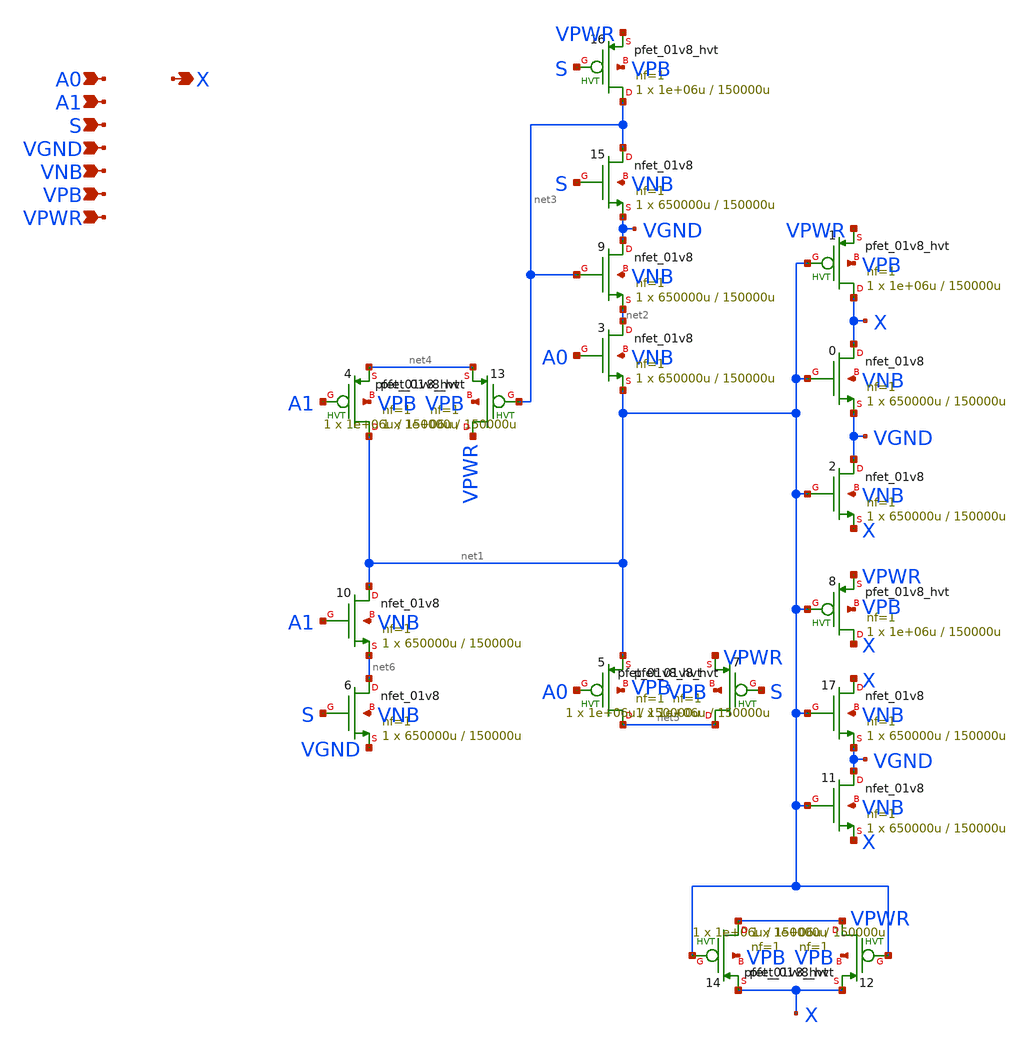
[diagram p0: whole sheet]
** sch_path: schematics/mux2/sky130_fd_sc_hd__mux2_4.sch
**.subckt sky130_fd_sc_hd__mux2_4 A0 A1 S VGND VNB VPB VPWR X
*.ipin A0
*.ipin A1
*.ipin S
*.ipin VGND
*.ipin VNB
*.ipin VPB
*.ipin VPWR
*.opin X
X0 X net1 VGND VNB sky130_fd_pr__nfet_01v8 L=150000u W=650000u nf=1 ad='int((1 + 1)/2) * 650000u / 1 * 0.29'
+ as='int((1 + 2)/2) * 650000u / 1 * 0.29' pd='2*int((1 + 1)/2) * (650000u / 1 + 0.29)' ps='2*int((1 + 2)/2) * (650000u / 1 + 0.29)'
+ nrd='0.29 / 650000u ' nrs='0.29 / 650000u ' sa=0 sb=0 sd=0 mult=1 m=1
X1 X net1 VPWR VPB sky130_fd_pr__pfet_01v8_hvt L=150000u W=1e+06u nf=1 ad='int((1 + 1)/2) * 1e+06u / 1 * 0.29'
+ as='int((1 + 2)/2) * 1e+06u / 1 * 0.29' pd='2*int((1 + 1)/2) * (1e+06u / 1 + 0.29)' ps='2*int((1 + 2)/2) * (1e+06u / 1 + 0.29)'
+ nrd='0.29 / 1e+06u ' nrs='0.29 / 1e+06u ' sa=0 sb=0 sd=0 mult=1 m=1
X2 VGND net1 X VNB sky130_fd_pr__nfet_01v8 L=150000u W=650000u nf=1 ad='int((1 + 1)/2) * 650000u / 1 * 0.29'
+ as='int((1 + 2)/2) * 650000u / 1 * 0.29' pd='2*int((1 + 1)/2) * (650000u / 1 + 0.29)' ps='2*int((1 + 2)/2) * (650000u / 1 + 0.29)'
+ nrd='0.29 / 650000u ' nrs='0.29 / 650000u ' sa=0 sb=0 sd=0 mult=1 m=1
X3 net2 A0 net1 VNB sky130_fd_pr__nfet_01v8 L=150000u W=650000u nf=1 ad='int((1 + 1)/2) * 650000u / 1 * 0.29'
+ as='int((1 + 2)/2) * 650000u / 1 * 0.29' pd='2*int((1 + 1)/2) * (650000u / 1 + 0.29)' ps='2*int((1 + 2)/2) * (650000u / 1 + 0.29)'
+ nrd='0.29 / 650000u ' nrs='0.29 / 650000u ' sa=0 sb=0 sd=0 mult=1 m=1
X4 net1 A1 net4 VPB sky130_fd_pr__pfet_01v8_hvt L=150000u W=1e+06u nf=1 ad='int((1 + 1)/2) * 1e+06u / 1 * 0.29'
+ as='int((1 + 2)/2) * 1e+06u / 1 * 0.29' pd='2*int((1 + 1)/2) * (1e+06u / 1 + 0.29)' ps='2*int((1 + 2)/2) * (1e+06u / 1 + 0.29)'
+ nrd='0.29 / 1e+06u ' nrs='0.29 / 1e+06u ' sa=0 sb=0 sd=0 mult=1 m=1
X9 VGND net3 net2 VNB sky130_fd_pr__nfet_01v8 L=150000u W=650000u nf=1 ad='int((1 + 1)/2) * 650000u / 1 * 0.29'
+ as='int((1 + 2)/2) * 650000u / 1 * 0.29' pd='2*int((1 + 1)/2) * (650000u / 1 + 0.29)' ps='2*int((1 + 2)/2) * (650000u / 1 + 0.29)'
+ nrd='0.29 / 650000u ' nrs='0.29 / 650000u ' sa=0 sb=0 sd=0 mult=1 m=1
X13 VPWR net3 net4 VPB sky130_fd_pr__pfet_01v8_hvt L=150000u W=1e+06u nf=1 ad='int((1 + 1)/2) * 1e+06u / 1 * 0.29'
+ as='int((1 + 2)/2) * 1e+06u / 1 * 0.29' pd='2*int((1 + 1)/2) * (1e+06u / 1 + 0.29)' ps='2*int((1 + 2)/2) * (1e+06u / 1 + 0.29)'
+ nrd='0.29 / 1e+06u ' nrs='0.29 / 1e+06u ' sa=0 sb=0 sd=0 mult=1 m=1
X15 net3 S VGND VNB sky130_fd_pr__nfet_01v8 L=150000u W=650000u nf=1 ad='int((1 + 1)/2) * 650000u / 1 * 0.29'
+ as='int((1 + 2)/2) * 650000u / 1 * 0.29' pd='2*int((1 + 1)/2) * (650000u / 1 + 0.29)' ps='2*int((1 + 2)/2) * (650000u / 1 + 0.29)'
+ nrd='0.29 / 650000u ' nrs='0.29 / 650000u ' sa=0 sb=0 sd=0 mult=1 m=1
X16 net3 S VPWR VPB sky130_fd_pr__pfet_01v8_hvt L=150000u W=1e+06u nf=1 ad='int((1 + 1)/2) * 1e+06u / 1 * 0.29'
+ as='int((1 + 2)/2) * 1e+06u / 1 * 0.29' pd='2*int((1 + 1)/2) * (1e+06u / 1 + 0.29)' ps='2*int((1 + 2)/2) * (1e+06u / 1 + 0.29)'
+ nrd='0.29 / 1e+06u ' nrs='0.29 / 1e+06u ' sa=0 sb=0 sd=0 mult=1 m=1
X5 net5 A0 net1 VPB sky130_fd_pr__pfet_01v8_hvt L=150000u W=1e+06u nf=1 ad='int((1 + 1)/2) * 1e+06u / 1 * 0.29'
+ as='int((1 + 2)/2) * 1e+06u / 1 * 0.29' pd='2*int((1 + 1)/2) * (1e+06u / 1 + 0.29)' ps='2*int((1 + 2)/2) * (1e+06u / 1 + 0.29)'
+ nrd='0.29 / 1e+06u ' nrs='0.29 / 1e+06u ' sa=0 sb=0 sd=0 mult=1 m=1
X7 net5 S VPWR VPB sky130_fd_pr__pfet_01v8_hvt L=150000u W=1e+06u nf=1 ad='int((1 + 1)/2) * 1e+06u / 1 * 0.29'
+ as='int((1 + 2)/2) * 1e+06u / 1 * 0.29' pd='2*int((1 + 1)/2) * (1e+06u / 1 + 0.29)' ps='2*int((1 + 2)/2) * (1e+06u / 1 + 0.29)'
+ nrd='0.29 / 1e+06u ' nrs='0.29 / 1e+06u ' sa=0 sb=0 sd=0 mult=1 m=1
X8 X net1 VPWR VPB sky130_fd_pr__pfet_01v8_hvt L=150000u W=1e+06u nf=1 ad='int((1 + 1)/2) * 1e+06u / 1 * 0.29'
+ as='int((1 + 2)/2) * 1e+06u / 1 * 0.29' pd='2*int((1 + 1)/2) * (1e+06u / 1 + 0.29)' ps='2*int((1 + 2)/2) * (1e+06u / 1 + 0.29)'
+ nrd='0.29 / 1e+06u ' nrs='0.29 / 1e+06u ' sa=0 sb=0 sd=0 mult=1 m=1
X11 VGND net1 X VNB sky130_fd_pr__nfet_01v8 L=150000u W=650000u nf=1 ad='int((1 + 1)/2) * 650000u / 1 * 0.29'
+ as='int((1 + 2)/2) * 650000u / 1 * 0.29' pd='2*int((1 + 1)/2) * (650000u / 1 + 0.29)' ps='2*int((1 + 2)/2) * (650000u / 1 + 0.29)'
+ nrd='0.29 / 650000u ' nrs='0.29 / 650000u ' sa=0 sb=0 sd=0 mult=1 m=1
X12 VPWR net1 X VPB sky130_fd_pr__pfet_01v8_hvt L=150000u W=1e+06u nf=1 ad='int((1 + 1)/2) * 1e+06u / 1 * 0.29'
+ as='int((1 + 2)/2) * 1e+06u / 1 * 0.29' pd='2*int((1 + 1)/2) * (1e+06u / 1 + 0.29)' ps='2*int((1 + 2)/2) * (1e+06u / 1 + 0.29)'
+ nrd='0.29 / 1e+06u ' nrs='0.29 / 1e+06u ' sa=0 sb=0 sd=0 mult=1 m=1
X14 VPWR net1 X VPB sky130_fd_pr__pfet_01v8_hvt L=150000u W=1e+06u nf=1 ad='int((1 + 1)/2) * 1e+06u / 1 * 0.29'
+ as='int((1 + 2)/2) * 1e+06u / 1 * 0.29' pd='2*int((1 + 1)/2) * (1e+06u / 1 + 0.29)' ps='2*int((1 + 2)/2) * (1e+06u / 1 + 0.29)'
+ nrd='0.29 / 1e+06u ' nrs='0.29 / 1e+06u ' sa=0 sb=0 sd=0 mult=1 m=1
X17 X net1 VGND VNB sky130_fd_pr__nfet_01v8 L=150000u W=650000u nf=1 ad='int((1 + 1)/2) * 650000u / 1 * 0.29'
+ as='int((1 + 2)/2) * 650000u / 1 * 0.29' pd='2*int((1 + 1)/2) * (650000u / 1 + 0.29)' ps='2*int((1 + 2)/2) * (650000u / 1 + 0.29)'
+ nrd='0.29 / 650000u ' nrs='0.29 / 650000u ' sa=0 sb=0 sd=0 mult=1 m=1
X6 net6 S VGND VNB sky130_fd_pr__nfet_01v8 L=150000u W=650000u nf=1 ad='int((1 + 1)/2) * 650000u / 1 * 0.29'
+ as='int((1 + 2)/2) * 650000u / 1 * 0.29' pd='2*int((1 + 1)/2) * (650000u / 1 + 0.29)' ps='2*int((1 + 2)/2) * (650000u / 1 + 0.29)'
+ nrd='0.29 / 650000u ' nrs='0.29 / 650000u ' sa=0 sb=0 sd=0 mult=1 m=1
X10 net1 A1 net6 VNB sky130_fd_pr__nfet_01v8 L=150000u W=650000u nf=1 ad='int((1 + 1)/2) * 650000u / 1 * 0.29'
+ as='int((1 + 2)/2) * 650000u / 1 * 0.29' pd='2*int((1 + 1)/2) * (650000u / 1 + 0.29)' ps='2*int((1 + 2)/2) * (650000u / 1 + 0.29)'
+ nrd='0.29 / 650000u ' nrs='0.29 / 650000u ' sa=0 sb=0 sd=0 mult=1 m=1
**.ends
.end
